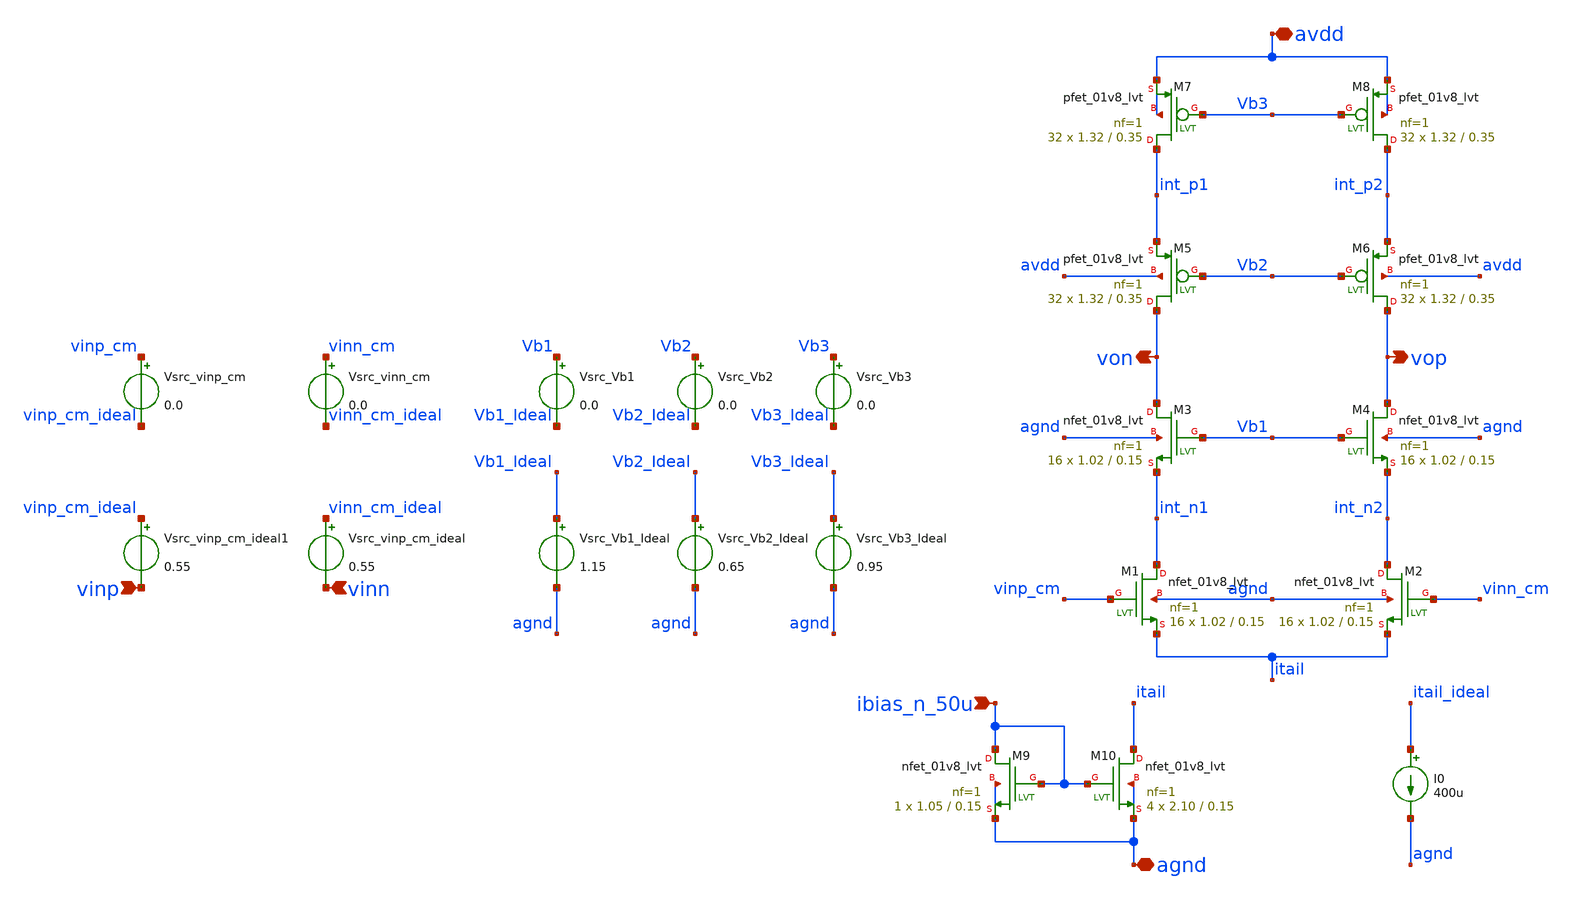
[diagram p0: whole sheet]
** sch_path: AMP/Final_Cascode_LVT.sch
**.subckt Final_Cascode_LVT avdd vinp vop agnd vinn von ibias_n_50u
*.iopin avdd
*.ipin vinp
*.opin vop
*.iopin agnd
*.ipin vinn
*.opin von
*.ipin ibias_n_50u
Vsrc_Vb3_Ideal Vb3_Ideal agnd 0.95
Vsrc_Vb2_Ideal Vb2_Ideal agnd 0.65
Vsrc_Vb1_Ideal Vb1_Ideal agnd 1.15
Vsrc_Vb3 Vb3 Vb3_Ideal 0.0
Vsrc_Vb2 Vb2 Vb2_Ideal 0.0
Vsrc_Vb1 Vb1 Vb1_Ideal 0.0
Vsrc_vinp_cm_ideal1 vinp_cm_ideal vinp 0.55
Vsrc_vinp_cm_ideal vinn_cm_ideal vinn 0.55
Vsrc_vinn_cm vinn_cm vinn_cm_ideal 0.0
Vsrc_vinp_cm vinp_cm vinp_cm_ideal 0.0
XM1 int_n1 vinp_cm itail agnd sky130_fd_pr__nfet_01v8_lvt L=0.15 W=1.02 nf=1 ad='int((nf+1)/2) * W/nf * 0.29'
+ as='int((nf+2)/2) * W/nf * 0.29' pd='2*int((nf+1)/2) * (W/nf + 0.29)' ps='2*int((nf+2)/2) * (W/nf + 0.29)'
+ nrd='0.29 / W' nrs='0.29 / W' sa=0 sb=0 sd=0 mult=16 m=16
XM2 int_n2 vinn_cm itail agnd sky130_fd_pr__nfet_01v8_lvt L=0.15 W=1.02 nf=1 ad='int((nf+1)/2) * W/nf * 0.29'
+ as='int((nf+2)/2) * W/nf * 0.29' pd='2*int((nf+1)/2) * (W/nf + 0.29)' ps='2*int((nf+2)/2) * (W/nf + 0.29)'
+ nrd='0.29 / W' nrs='0.29 / W' sa=0 sb=0 sd=0 mult=16 m=16
XM3 von Vb1 int_n1 agnd sky130_fd_pr__nfet_01v8_lvt L=0.15 W=1.02 nf=1 ad='int((nf+1)/2) * W/nf * 0.29'
+ as='int((nf+2)/2) * W/nf * 0.29' pd='2*int((nf+1)/2) * (W/nf + 0.29)' ps='2*int((nf+2)/2) * (W/nf + 0.29)'
+ nrd='0.29 / W' nrs='0.29 / W' sa=0 sb=0 sd=0 mult=16 m=16
XM4 vop Vb1 int_n2 agnd sky130_fd_pr__nfet_01v8_lvt L=0.15 W=1.02 nf=1 ad='int((nf+1)/2) * W/nf * 0.29'
+ as='int((nf+2)/2) * W/nf * 0.29' pd='2*int((nf+1)/2) * (W/nf + 0.29)' ps='2*int((nf+2)/2) * (W/nf + 0.29)'
+ nrd='0.29 / W' nrs='0.29 / W' sa=0 sb=0 sd=0 mult=16 m=16
XM5 von Vb2 int_p1 avdd sky130_fd_pr__pfet_01v8_lvt L=0.35 W=1.32 nf=1 ad='int((nf+1)/2) * W/nf * 0.29'
+ as='int((nf+2)/2) * W/nf * 0.29' pd='2*int((nf+1)/2) * (W/nf + 0.29)' ps='2*int((nf+2)/2) * (W/nf + 0.29)'
+ nrd='0.29 / W' nrs='0.29 / W' sa=0 sb=0 sd=0 mult=32 m=32
XM6 vop Vb2 int_p2 avdd sky130_fd_pr__pfet_01v8_lvt L=0.35 W=1.32 nf=1 ad='int((nf+1)/2) * W/nf * 0.29'
+ as='int((nf+2)/2) * W/nf * 0.29' pd='2*int((nf+1)/2) * (W/nf + 0.29)' ps='2*int((nf+2)/2) * (W/nf + 0.29)'
+ nrd='0.29 / W' nrs='0.29 / W' sa=0 sb=0 sd=0 mult=32 m=32
XM7 int_p1 Vb3 avdd avdd sky130_fd_pr__pfet_01v8_lvt L=0.35 W=1.32 nf=1 ad='int((nf+1)/2) * W/nf * 0.29'
+ as='int((nf+2)/2) * W/nf * 0.29' pd='2*int((nf+1)/2) * (W/nf + 0.29)' ps='2*int((nf+2)/2) * (W/nf + 0.29)'
+ nrd='0.29 / W' nrs='0.29 / W' sa=0 sb=0 sd=0 mult=32 m=32
XM8 int_p2 Vb3 avdd avdd sky130_fd_pr__pfet_01v8_lvt L=0.35 W=1.32 nf=1 ad='int((nf+1)/2) * W/nf * 0.29'
+ as='int((nf+2)/2) * W/nf * 0.29' pd='2*int((nf+1)/2) * (W/nf + 0.29)' ps='2*int((nf+2)/2) * (W/nf + 0.29)'
+ nrd='0.29 / W' nrs='0.29 / W' sa=0 sb=0 sd=0 mult=32 m=32
XM9 ibias_n_50u ibias_n_50u agnd agnd sky130_fd_pr__nfet_01v8_lvt L=0.15 W=1.05 nf=1 ad='int((nf+1)/2) * W/nf * 0.29'
+ as='int((nf+2)/2) * W/nf * 0.29' pd='2*int((nf+1)/2) * (W/nf + 0.29)' ps='2*int((nf+2)/2) * (W/nf + 0.29)'
+ nrd='0.29 / W' nrs='0.29 / W' sa=0 sb=0 sd=0 mult=1 m=1
XM10 itail ibias_n_50u agnd agnd sky130_fd_pr__nfet_01v8_lvt L=0.15 W=2.10 nf=1 ad='int((nf+1)/2) * W/nf * 0.29'
+ as='int((nf+2)/2) * W/nf * 0.29' pd='2*int((nf+1)/2) * (W/nf + 0.29)' ps='2*int((nf+2)/2) * (W/nf + 0.29)'
+ nrd='0.29 / W' nrs='0.29 / W' sa=0 sb=0 sd=0 mult=4 m=4
I0 itail_ideal agnd 400u
**.ends
.end
